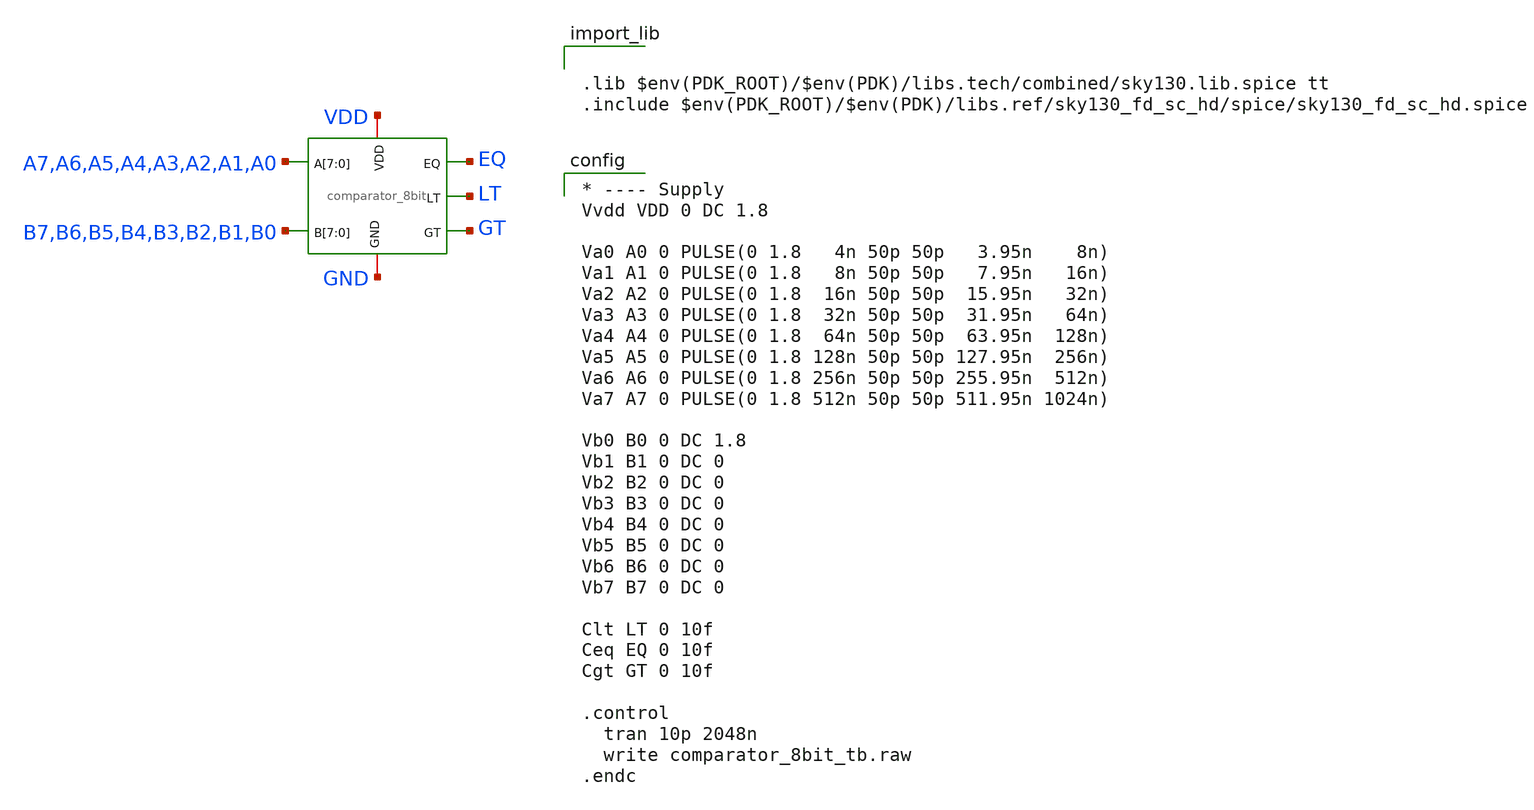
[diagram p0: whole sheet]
** sch_path: xschem/comparator_8bit_tb.sch
**.subckt comparator_8bit_tb
x1 VDD EQ A7 A6 A5 A4 A3 A2 A1 A0 LT GND B7 B6 B5 B4 B3 B2 B1 B0 GT comparator_8bit
**** begin user architecture code


.lib $env(PDK_ROOT)/$env(PDK)/libs.tech/combined/sky130.lib.spice tt
.include $env(PDK_ROOT)/$env(PDK)/libs.ref/sky130_fd_sc_hd/spice/sky130_fd_sc_hd.spice



* ---- Supply
Vvdd VDD 0 DC 1.8

Va0 A0 0 PULSE(0 1.8   4n 50p 50p   3.95n    8n)
Va1 A1 0 PULSE(0 1.8   8n 50p 50p   7.95n   16n)
Va2 A2 0 PULSE(0 1.8  16n 50p 50p  15.95n   32n)
Va3 A3 0 PULSE(0 1.8  32n 50p 50p  31.95n   64n)
Va4 A4 0 PULSE(0 1.8  64n 50p 50p  63.95n  128n)
Va5 A5 0 PULSE(0 1.8 128n 50p 50p 127.95n  256n)
Va6 A6 0 PULSE(0 1.8 256n 50p 50p 255.95n  512n)
Va7 A7 0 PULSE(0 1.8 512n 50p 50p 511.95n 1024n)

Vb0 B0 0 DC 1.8
Vb1 B1 0 DC 0
Vb2 B2 0 DC 0
Vb3 B3 0 DC 0
Vb4 B4 0 DC 0
Vb5 B5 0 DC 0
Vb6 B6 0 DC 0
Vb7 B7 0 DC 0

Clt LT 0 10f
Ceq EQ 0 10f
Cgt GT 0 10f

.control
  tran 10p 2048n
  write comparator_8bit_tb.raw
.endc

**** end user architecture code
**.ends

* expanding   symbol:  comparator_8bit.sym # of pins=7
** sym_path: xschem/comparator_8bit.sym
** sch_path: xschem/comparator_8bit.sch
.subckt comparator_8bit VDD EQ A[7] A[6] A[5] A[4] A[3] A[2] A[1] A[0] LT GND B[7] B[6] B[5] B[4]
+ B[3] B[2] B[1] B[0] GT
*.opin EQ
*.opin LT
*.opin GT
*.iopin VDD
*.iopin GND
*.ipin A[7],A[6],A[5],A[4],A[3],A[2],A[1],A[0]
*.ipin B[7],B[6],B[5],B[4],B[3],B[2],B[1],B[0]
x2 A[1] net1 E1 GND GND VDD VDD net2 sky130_fd_sc_hd__mux2i_1
x3 B[2] net2 E2 GND GND VDD VDD net3 sky130_fd_sc_hd__mux2i_1
x4 A[3] net3 E3 GND GND VDD VDD net7 sky130_fd_sc_hd__mux2i_1
x6 A[5] net4 E5 GND GND VDD VDD net5 sky130_fd_sc_hd__mux2i_1
x7 B[6] net5 E6 GND GND VDD VDD net6 sky130_fd_sc_hd__mux2i_1
x8 B[7] net6 E7 GND GND VDD VDD net8 sky130_fd_sc_hd__mux2i_1
x9 E0 E1 E2 E3 GND GND VDD VDD NLO sky130_fd_sc_hd__nand4_1
x11 A[0] B[0] GND GND VDD VDD E0 sky130_fd_sc_hd__xnor2_1
x10 E4 E5 E6 E7 GND GND VDD VDD NHI sky130_fd_sc_hd__nand4_1
x19 NLO NHI GND GND VDD VDD EQ sky130_fd_sc_hd__nor2_1
x20 net7 net8 NHI GND GND VDD VDD GT sky130_fd_sc_hd__mux2i_1
x21 EQ GT GND GND VDD VDD LT sky130_fd_sc_hd__nor2_1
x12 A[1] B[1] GND GND VDD VDD E1 sky130_fd_sc_hd__xnor2_1
x13 A[2] B[2] GND GND VDD VDD E2 sky130_fd_sc_hd__xnor2_1
x14 A[3] B[3] GND GND VDD VDD E3 sky130_fd_sc_hd__xnor2_1
x15 A[4] B[4] GND GND VDD VDD E4 sky130_fd_sc_hd__xnor2_1
x16 A[5] B[5] GND GND VDD VDD E5 sky130_fd_sc_hd__xnor2_1
x17 A[6] B[6] GND GND VDD VDD E6 sky130_fd_sc_hd__xnor2_1
x18 A[7] B[7] GND GND VDD VDD E7 sky130_fd_sc_hd__xnor2_1
x22 B[0] A[0] GND GND VDD VDD net1 sky130_fd_sc_hd__nor2b_1
x1 B[4] A[4] GND GND VDD VDD net4 sky130_fd_sc_hd__nor2b_1
.ends

.end
